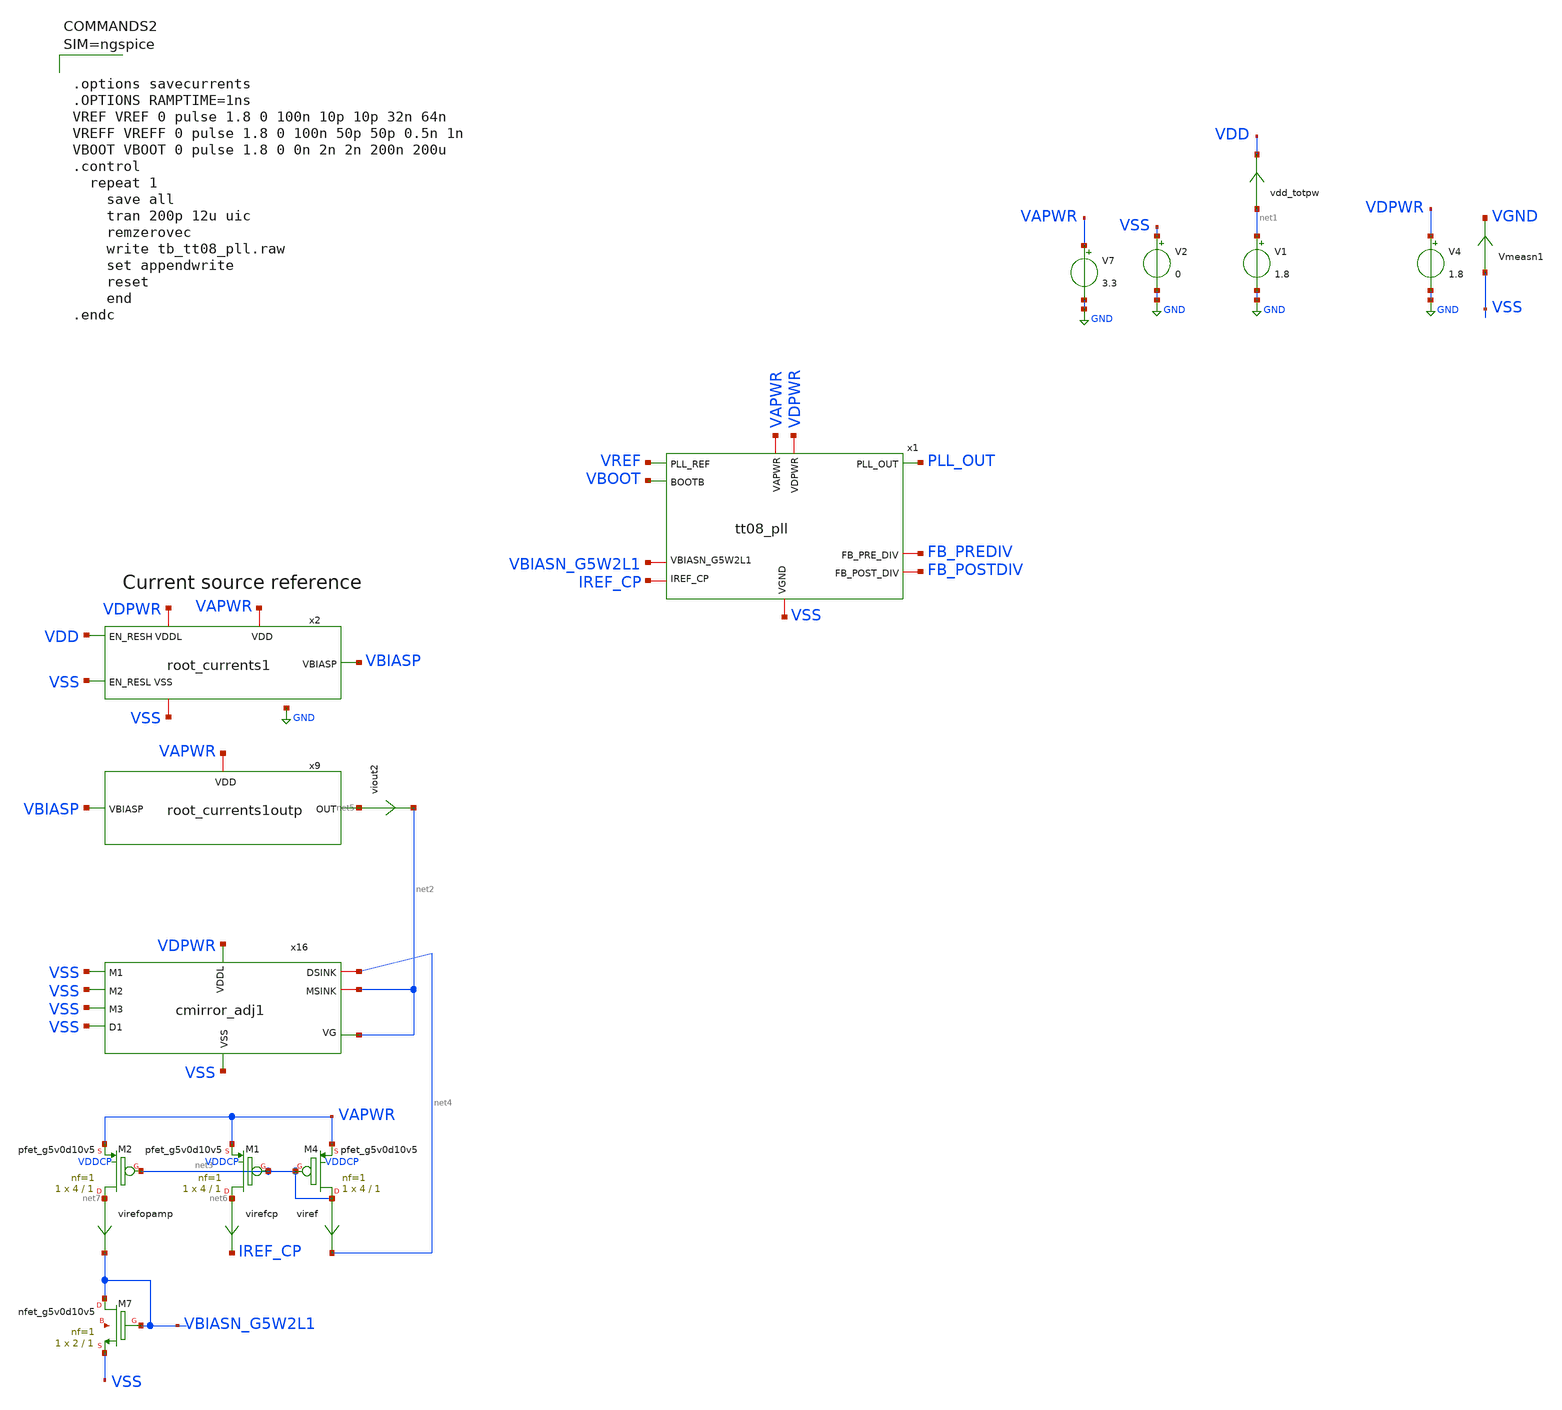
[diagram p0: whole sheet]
** sch_path: xschem/tb_tt08_pll.sch
**.subckt tb_tt08_pll
V1 net1 GND 1.8
V2 VSS GND 0
vdd_totpw net1 VDD 0
.save i(vdd_totpw)
Vmeasn1 VSS VGND 0
.save i(vmeasn1)
V4 VDPWR GND 1.8
V7 VAPWR GND 3.3
x2 VDD VSS VBIASP VAPWR VDPWR VSS root_currents1
x9 VBIASP net5 VAPWR root_currents1outp
viout2 net5 net2 0
.save i(viout2)
x16 VSS VSS VSS VSS VDPWR VSS net2 net4 net2 cmirror_adj1
viref net3 net4 0
.save i(viref)
XM4 net3 net3 VAPWR VDDCP sky130_fd_pr__pfet_g5v0d10v5 L=1 W=4 nf=1 ad='int((nf+1)/2) * W/nf * 0.29'
+ as='int((nf+2)/2) * W/nf * 0.29' pd='2*int((nf+1)/2) * (W/nf + 0.29)' ps='2*int((nf+2)/2) * (W/nf + 0.29)'
+ nrd='0.29 / W' nrs='0.29 / W' sa=0 sb=0 sd=0 mult=1 m=1
virefcp net6 IREF_CP 0
.save i(virefcp)
XM1 net6 net3 VAPWR VDDCP sky130_fd_pr__pfet_g5v0d10v5 L=1 W=4 nf=1 ad='int((nf+1)/2) * W/nf * 0.29'
+ as='int((nf+2)/2) * W/nf * 0.29' pd='2*int((nf+1)/2) * (W/nf + 0.29)' ps='2*int((nf+2)/2) * (W/nf + 0.29)'
+ nrd='0.29 / W' nrs='0.29 / W' sa=0 sb=0 sd=0 mult=1 m=1
virefopamp net7 VBIASN_G5W2L1 0
.save i(virefopamp)
XM2 net7 net3 VAPWR VDDCP sky130_fd_pr__pfet_g5v0d10v5 L=1 W=4 nf=1 ad='int((nf+1)/2) * W/nf * 0.29'
+ as='int((nf+2)/2) * W/nf * 0.29' pd='2*int((nf+1)/2) * (W/nf + 0.29)' ps='2*int((nf+2)/2) * (W/nf + 0.29)'
+ nrd='0.29 / W' nrs='0.29 / W' sa=0 sb=0 sd=0 mult=1 m=1
XM7 VBIASN_G5W2L1 VBIASN_G5W2L1 VSS net8 sky130_fd_pr__nfet_g5v0d10v5 L=1 W=2 nf=1 ad='int((nf+1)/2) * W/nf * 0.29'
+ as='int((nf+2)/2) * W/nf * 0.29' pd='2*int((nf+1)/2) * (W/nf + 0.29)' ps='2*int((nf+2)/2) * (W/nf + 0.29)'
+ nrd='0.29 / W' nrs='0.29 / W' sa=0 sb=0 sd=0 mult=1 m=1
x1 VREF VBOOT PLL_OUT FB_PREDIV FB_POSTDIV VBIASN_G5W2L1 IREF_CP VAPWR VDPWR VSS tt08_pll
**** begin user architecture code

** opencircuitdesign pdks install
.lib $::SKYWATER_MODELS/sky130.lib.spice tt
.include $::SKYWATER_STDCELLS/sky130_fd_sc_hd.spice





.options savecurrents
.OPTIONS RAMPTIME=1ns
VREF VREF 0 pulse 1.8 0 100n 10p 10p 32n 64n
VREFF VREFF 0 pulse 1.8 0 100n 50p 50p 0.5n 1n
VBOOT VBOOT 0 pulse 1.8 0 0n 2n 2n 200n 200u
.control
  repeat 1
    save all
    tran 200p 12u uic
    remzerovec
    write tb_tt08_pll.raw
    set appendwrite
    reset
    end
.endc



**** end user architecture code
**.ends
.GLOBAL GND
.end
